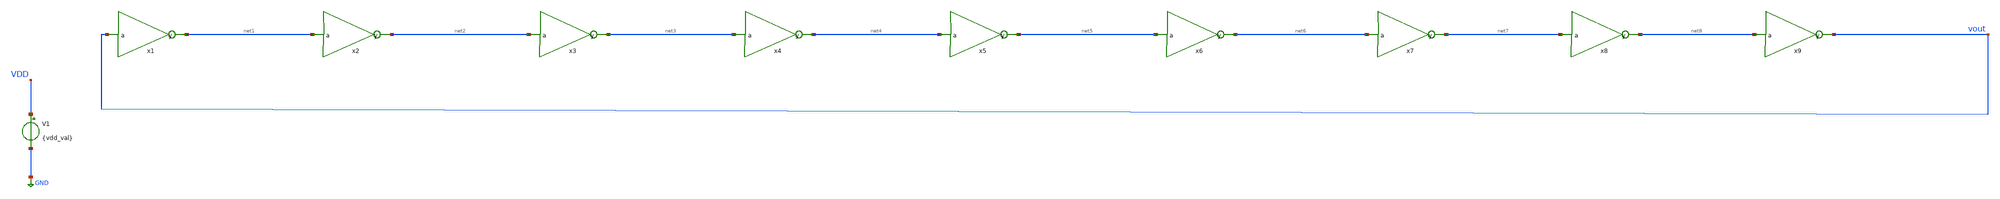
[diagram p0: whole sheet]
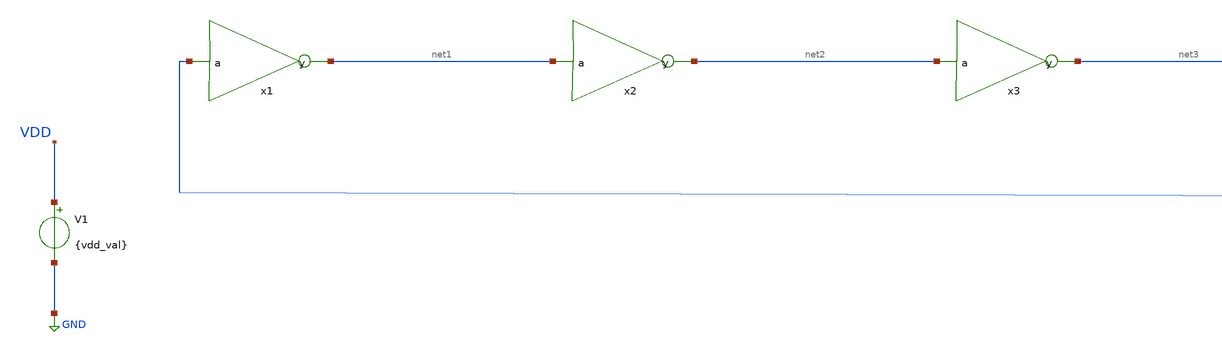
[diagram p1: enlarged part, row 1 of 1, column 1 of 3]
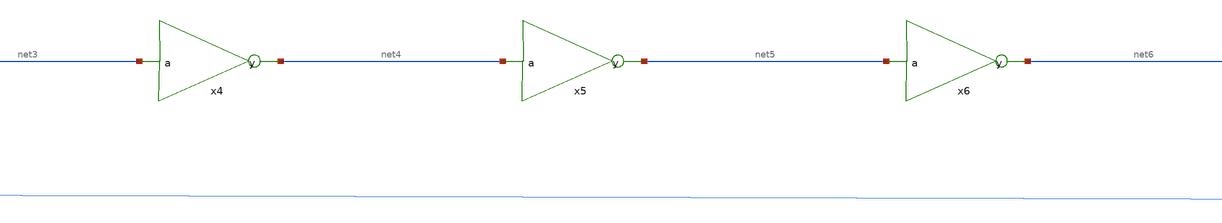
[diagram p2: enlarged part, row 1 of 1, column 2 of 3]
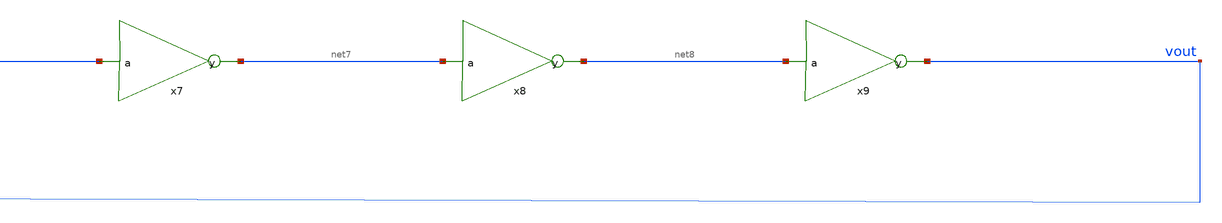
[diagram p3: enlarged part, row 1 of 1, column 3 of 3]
** sch_path: assignments/assignment3/assign2c.sch
**.subckt assign2c
x1 net1 vout inverter
x2 net2 net1 inverter
x3 net3 net2 inverter
x4 net4 net3 inverter
x5 net5 net4 inverter
x6 net6 net5 inverter
x7 net7 net6 inverter
V1 VDD GND {vdd_val}
x8 net8 net7 inverter
x9 vout net8 inverter
**** begin user architecture code


.param vdd_val = 1.8
.param width_p = 0.84

.ic v(vout)=0

.control

let Nsim = 9
let periodvec = vector(Nsim)
let freqvec = vector(Nsim)
let vddvec = vector(Nsim)
let index = 0

while index < Nsim

  let vddv = 1.0 + (index * 0.1)
  alterparam vdd_val = $&vddv

  reset
  * Give it plenty of time (40ns) so 1.0V and 1.1V fully settle

  * Give it a massive window (100ns) so 1.0V can easily hit 5 edges
  tran 1p 100n uic

  meas tran t1 WHEN v(vout)=0.4 rise=4
  meas tran t2 WHEN v(vout)=0.4 rise=5

  let periodvec[index] = t2 - t1
  let freqvec[index] = 1 / (t2 - t1)
  let vddvec[index] = vddv
  let index = index + 1

end

plot freqvec vs vddvec
plot periodvec vs vddvec


.endc


.lib $::SKYWATER_MODELS/sky130.lib.spice tt
**** end user architecture code
**.ends

* expanding   symbol:  inverter.sym # of pins=2
** sym_path: assignments/assignment3/inverter.sym
** sch_path: assignments/assignment3/inverter.sch
.subckt inverter y a
*.ipin a
*.opin y
XM1 y a GND GND sky130_fd_pr__nfet_01v8 L=0.15 W=0.42 nf=1 ad='int((nf+1)/2) * W/nf * 0.29' as='int((nf+2)/2) * W/nf * 0.29'
+ pd='2*int((nf+1)/2) * (W/nf + 0.29)' ps='2*int((nf+2)/2) * (W/nf + 0.29)' nrd='0.29 / W' nrs='0.29 / W'
+ sa=0 sb=0 sd=0 mult=1 m=1
XM2 y a VDD VDD sky130_fd_pr__pfet_01v8 L=0.15 W={width_p} nf=1 ad='int((nf+1)/2) * W/nf * 0.29' as='int((nf+2)/2) * W/nf * 0.29'
+ pd='2*int((nf+1)/2) * (W/nf + 0.29)' ps='2*int((nf+2)/2) * (W/nf + 0.29)' nrd='0.29 / W' nrs='0.29 / W'
+ sa=0 sb=0 sd=0 mult=1 m=1
.ends

.GLOBAL GND
.GLOBAL VDD
.end
